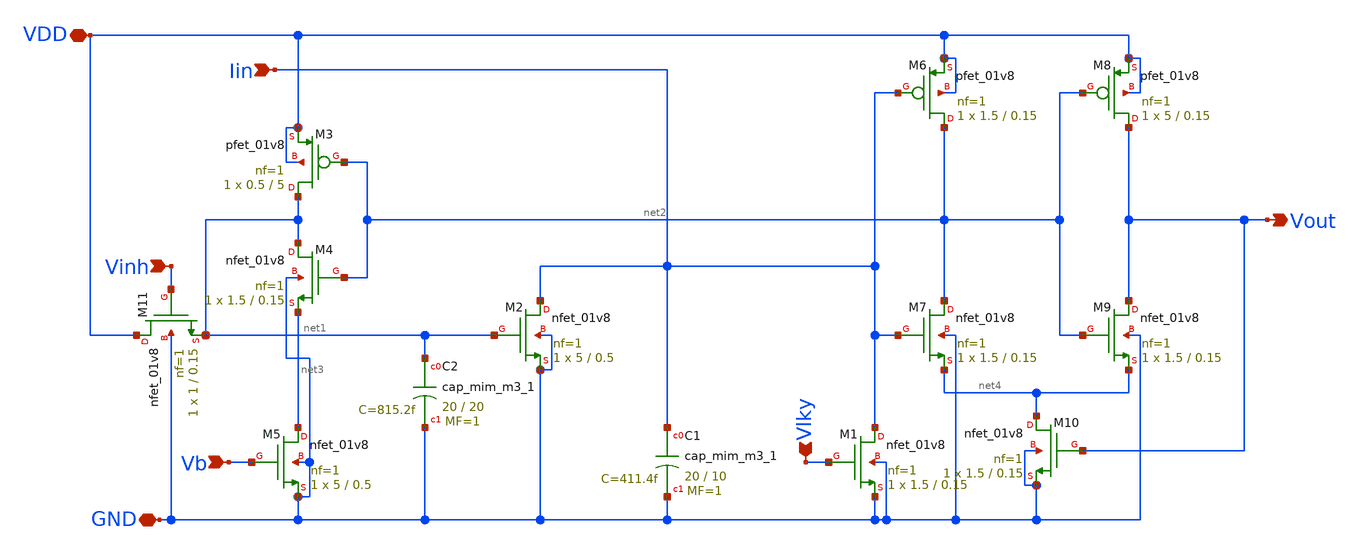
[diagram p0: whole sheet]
** sch_path: Final_Design/Output_LIF.sch
**.subckt Output_LIF GND Vb VDD Vout Iin Vlky Vinh
*.iopin GND
*.ipin Vb
*.iopin VDD
*.opin Vout
*.ipin Iin
*.ipin Vlky
*.ipin Vinh
XM5 net3 Vb GND GND sky130_fd_pr__nfet_01v8 L=0.5 W=5 nf=1 ad='int((nf+1)/2) * W/nf * 0.29' as='int((nf+2)/2) * W/nf * 0.29'
+ pd='2*int((nf+1)/2) * (W/nf + 0.29)' ps='2*int((nf+2)/2) * (W/nf + 0.29)' nrd='0.29 / W' nrs='0.29 / W'
+ sa=0 sb=0 sd=0 mult=1 m=1
XM4 net1 net2 net3 GND sky130_fd_pr__nfet_01v8 L=0.15 W=1.5 nf=1 ad='int((nf+1)/2) * W/nf * 0.29' as='int((nf+2)/2) * W/nf * 0.29'
+ pd='2*int((nf+1)/2) * (W/nf + 0.29)' ps='2*int((nf+2)/2) * (W/nf + 0.29)' nrd='0.29 / W' nrs='0.29 / W'
+ sa=0 sb=0 sd=0 mult=1 m=1
XM3 net1 net2 VDD VDD sky130_fd_pr__pfet_01v8 L=5 W=0.5 nf=1 ad='int((nf+1)/2) * W/nf * 0.29' as='int((nf+2)/2) * W/nf * 0.29'
+ pd='2*int((nf+1)/2) * (W/nf + 0.29)' ps='2*int((nf+2)/2) * (W/nf + 0.29)' nrd='0.29 / W' nrs='0.29 / W'
+ sa=0 sb=0 sd=0 mult=1 m=1
XC2 net1 GND sky130_fd_pr__cap_mim_m3_1 W=20 L=20 MF=1 m=1
XM2 Iin net1 GND GND sky130_fd_pr__nfet_01v8 L=0.5 W=5 nf=1 ad='int((nf+1)/2) * W/nf * 0.29' as='int((nf+2)/2) * W/nf * 0.29'
+ pd='2*int((nf+1)/2) * (W/nf + 0.29)' ps='2*int((nf+2)/2) * (W/nf + 0.29)' nrd='0.29 / W' nrs='0.29 / W'
+ sa=0 sb=0 sd=0 mult=1 m=1
XC1 Iin GND sky130_fd_pr__cap_mim_m3_1 W=20 L=10 MF=1 m=1
XM10 net4 Vout GND GND sky130_fd_pr__nfet_01v8 L=0.15 W=1.5 nf=1 ad='int((nf+1)/2) * W/nf * 0.29' as='int((nf+2)/2) * W/nf * 0.29'
+ pd='2*int((nf+1)/2) * (W/nf + 0.29)' ps='2*int((nf+2)/2) * (W/nf + 0.29)' nrd='0.29 / W' nrs='0.29 / W'
+ sa=0 sb=0 sd=0 mult=1 m=1
XM7 net2 Iin net4 GND sky130_fd_pr__nfet_01v8 L=0.15 W=1.5 nf=1 ad='int((nf+1)/2) * W/nf * 0.29' as='int((nf+2)/2) * W/nf * 0.29'
+ pd='2*int((nf+1)/2) * (W/nf + 0.29)' ps='2*int((nf+2)/2) * (W/nf + 0.29)' nrd='0.29 / W' nrs='0.29 / W'
+ sa=0 sb=0 sd=0 mult=1 m=1
XM6 net2 Iin VDD VDD sky130_fd_pr__pfet_01v8 L=0.15 W=1.5 nf=1 ad='int((nf+1)/2) * W/nf * 0.29' as='int((nf+2)/2) * W/nf * 0.29'
+ pd='2*int((nf+1)/2) * (W/nf + 0.29)' ps='2*int((nf+2)/2) * (W/nf + 0.29)' nrd='0.29 / W' nrs='0.29 / W'
+ sa=0 sb=0 sd=0 mult=1 m=1
XM9 Vout net2 net4 GND sky130_fd_pr__nfet_01v8 L=0.15 W=1.5 nf=1 ad='int((nf+1)/2) * W/nf * 0.29' as='int((nf+2)/2) * W/nf * 0.29'
+ pd='2*int((nf+1)/2) * (W/nf + 0.29)' ps='2*int((nf+2)/2) * (W/nf + 0.29)' nrd='0.29 / W' nrs='0.29 / W'
+ sa=0 sb=0 sd=0 mult=1 m=1
XM8 Vout net2 VDD VDD sky130_fd_pr__pfet_01v8 L=0.15 W=5 nf=1 ad='int((nf+1)/2) * W/nf * 0.29' as='int((nf+2)/2) * W/nf * 0.29'
+ pd='2*int((nf+1)/2) * (W/nf + 0.29)' ps='2*int((nf+2)/2) * (W/nf + 0.29)' nrd='0.29 / W' nrs='0.29 / W'
+ sa=0 sb=0 sd=0 mult=1 m=1
XM1 Iin Vlky GND GND sky130_fd_pr__nfet_01v8 L=0.15 W=1.5 nf=1 ad='int((nf+1)/2) * W/nf * 0.29' as='int((nf+2)/2) * W/nf * 0.29'
+ pd='2*int((nf+1)/2) * (W/nf + 0.29)' ps='2*int((nf+2)/2) * (W/nf + 0.29)' nrd='0.29 / W' nrs='0.29 / W'
+ sa=0 sb=0 sd=0 mult=1 m=1
XM11 VDD Vinh net1 GND sky130_fd_pr__nfet_01v8 L=0.15 W=1 nf=1 ad='int((nf+1)/2) * W/nf * 0.29' as='int((nf+2)/2) * W/nf * 0.29'
+ pd='2*int((nf+1)/2) * (W/nf + 0.29)' ps='2*int((nf+2)/2) * (W/nf + 0.29)' nrd='0.29 / W' nrs='0.29 / W'
+ sa=0 sb=0 sd=0 mult=1 m=1
**.ends
.end
